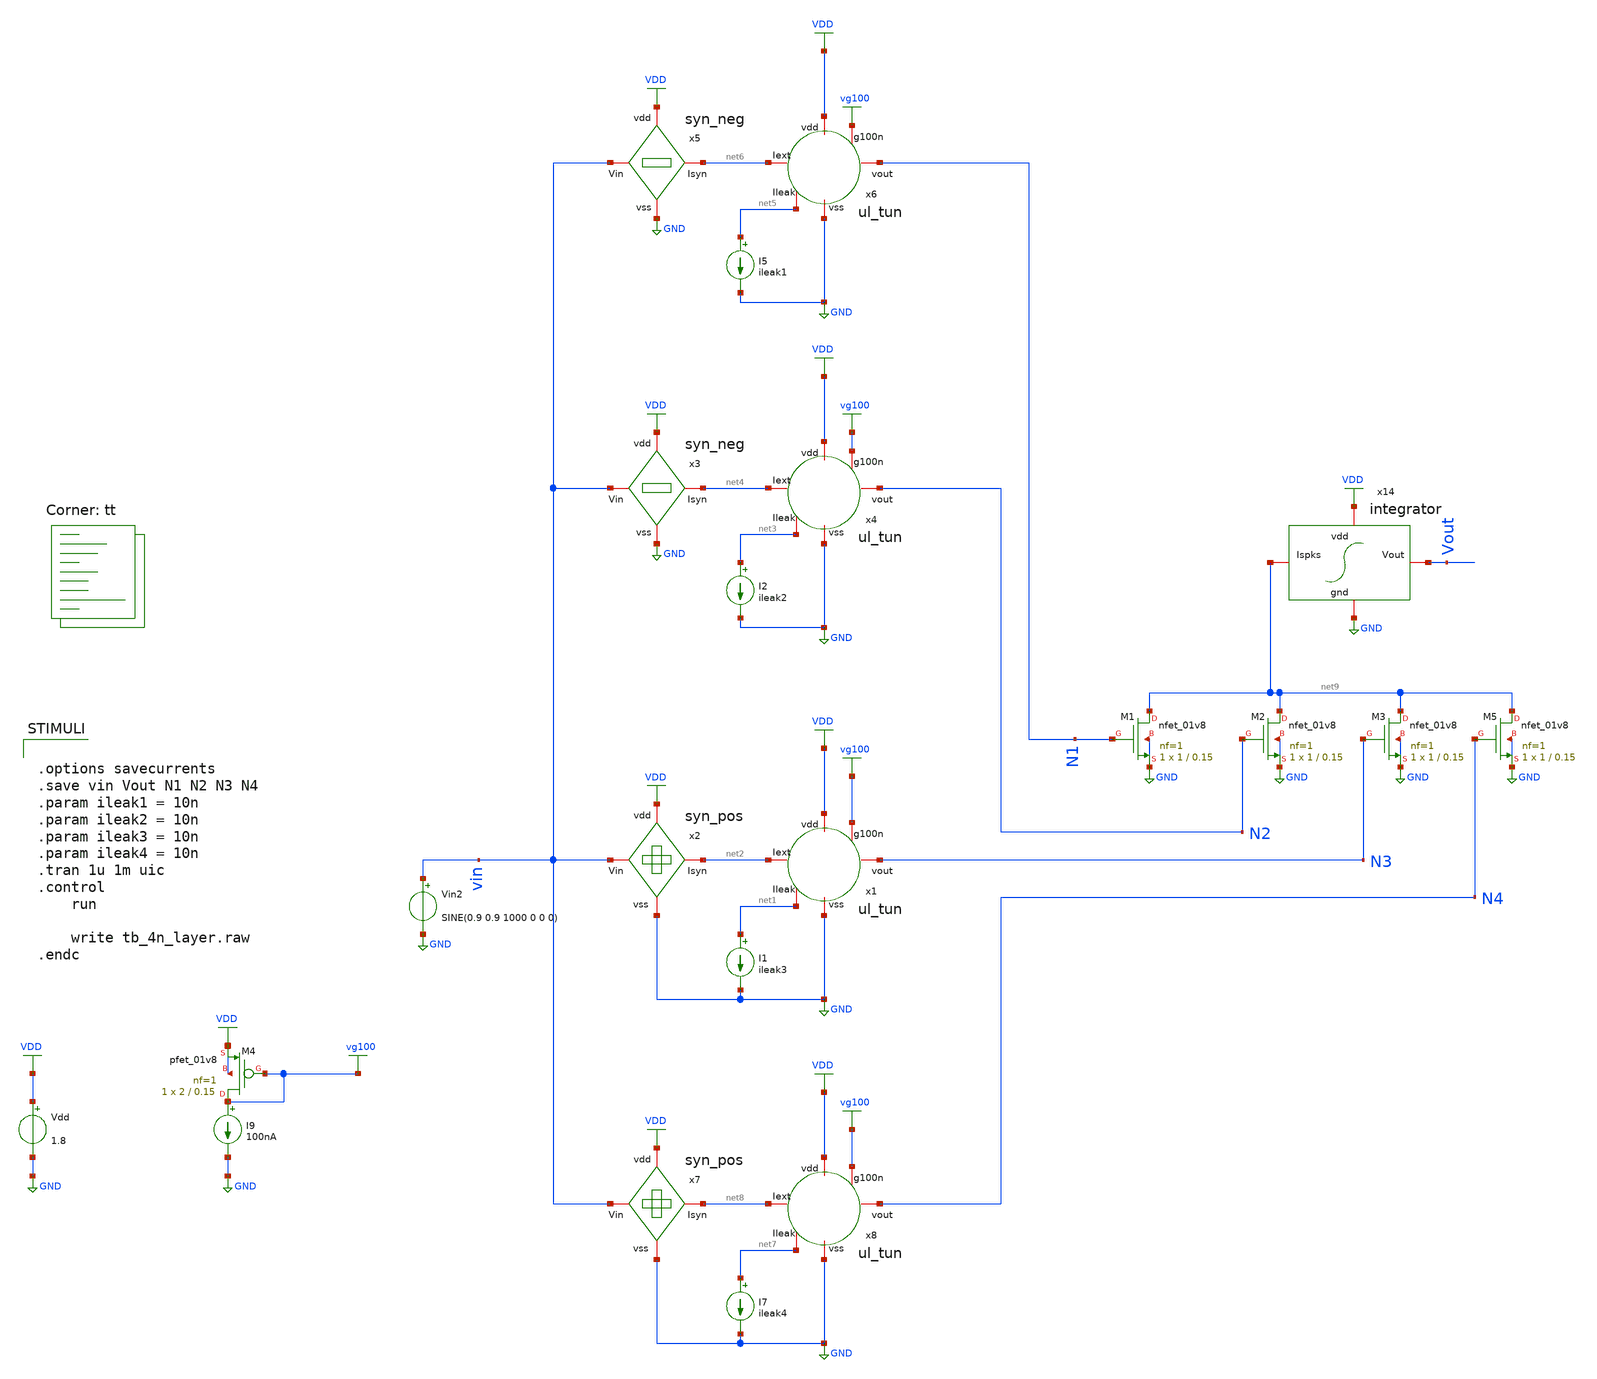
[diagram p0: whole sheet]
** sch_path: Neuron/ultralif/tb_4n_layer.sch
**.subckt tb_4n_layer
I1 net1 GND ileak3
Vdd VDD GND 1.8
x2 VDD vin net2 GND syn_pos
x1 net2 VDD vg100 N3 net1 GND ul_tun
I2 net3 GND ileak2
x3 VDD vin net4 GND syn_neg
x4 net4 VDD vg100 N2 net3 GND ul_tun
I5 net5 GND ileak1
x5 VDD vin net6 GND syn_neg
x6 net6 VDD vg100 N1 net5 GND ul_tun
I7 net7 GND ileak4
x7 VDD vin net8 GND syn_pos
x8 net8 VDD vg100 N4 net7 GND ul_tun
I9 vg100 GND 100nA
XM4 vg100 vg100 VDD VDD sky130_fd_pr__pfet_01v8 L=0.15 W=2 nf=1 ad='int((nf+1)/2) * W/nf * 0.29' as='int((nf+2)/2) * W/nf * 0.29'
+ pd='2*int((nf+1)/2) * (W/nf + 0.29)' ps='2*int((nf+2)/2) * (W/nf + 0.29)' nrd='0.29 / W' nrs='0.29 / W'
+ sa=0 sb=0 sd=0 mult=1 m=1
x14 VDD Vout net9 GND integrator
XM1 net9 N1 GND GND sky130_fd_pr__nfet_01v8 L=0.15 W=1 nf=1 ad='int((nf+1)/2) * W/nf * 0.29' as='int((nf+2)/2) * W/nf * 0.29'
+ pd='2*int((nf+1)/2) * (W/nf + 0.29)' ps='2*int((nf+2)/2) * (W/nf + 0.29)' nrd='0.29 / W' nrs='0.29 / W'
+ sa=0 sb=0 sd=0 mult=1 m=1
XM2 net9 N2 GND GND sky130_fd_pr__nfet_01v8 L=0.15 W=1 nf=1 ad='int((nf+1)/2) * W/nf * 0.29' as='int((nf+2)/2) * W/nf * 0.29'
+ pd='2*int((nf+1)/2) * (W/nf + 0.29)' ps='2*int((nf+2)/2) * (W/nf + 0.29)' nrd='0.29 / W' nrs='0.29 / W'
+ sa=0 sb=0 sd=0 mult=1 m=1
XM3 net9 N3 GND GND sky130_fd_pr__nfet_01v8 L=0.15 W=1 nf=1 ad='int((nf+1)/2) * W/nf * 0.29' as='int((nf+2)/2) * W/nf * 0.29'
+ pd='2*int((nf+1)/2) * (W/nf + 0.29)' ps='2*int((nf+2)/2) * (W/nf + 0.29)' nrd='0.29 / W' nrs='0.29 / W'
+ sa=0 sb=0 sd=0 mult=1 m=1
XM5 net9 N4 GND GND sky130_fd_pr__nfet_01v8 L=0.15 W=1 nf=1 ad='int((nf+1)/2) * W/nf * 0.29' as='int((nf+2)/2) * W/nf * 0.29'
+ pd='2*int((nf+1)/2) * (W/nf + 0.29)' ps='2*int((nf+2)/2) * (W/nf + 0.29)' nrd='0.29 / W' nrs='0.29 / W'
+ sa=0 sb=0 sd=0 mult=1 m=1
Vin2 vin GND SINE(0.9 0.9 1000 0 0 0)
**** begin user architecture code
.lib $::SKYWATER_MODELS/sky130.lib.spice tt
**** end user architecture code
**.ends
.GLOBAL GND
.GLOBAL VDD
.GLOBAL vg100
**** begin user architecture code


.options savecurrents
.save vin Vout N1 N2 N3 N4
.param ileak1 = 10n
.param ileak2 = 10n
.param ileak3 = 10n
.param ileak4 = 10n
.tran 1u 1m uic
.control
	run

	write tb_4n_layer.raw
.endc


**** end user architecture code
.end
